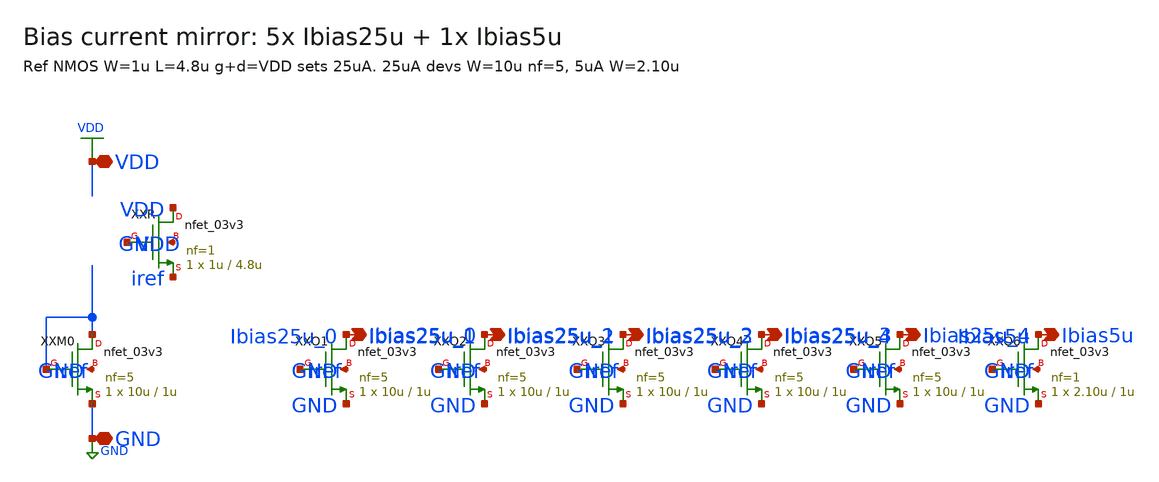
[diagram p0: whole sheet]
** sch_path: ps-bias/bias.sch
**.subckt bias Ibias25u_0 Ibias25u_1 Ibias25u_2 Ibias25u_3 Ibias25u_4 Ibias5u VDD GND
*.opin Ibias25u_0
*.opin Ibias25u_1
*.opin Ibias25u_2
*.opin Ibias25u_3
*.opin Ibias25u_4
*.opin Ibias5u
*.iopin VDD
*.iopin GND
XXR VDD VDD iref GND nfet_03v3 L=4.8u W=1u nf=1 ad='int((nf+1)/2) * W/nf * 0.18u' as='int((nf+2)/2) * W/nf * 0.18u'
+ pd='2*int((nf+1)/2) * (W/nf + 0.18u)' ps='2*int((nf+2)/2) * (W/nf + 0.18u)' nrd='0.18u / W' nrs='0.18u / W'
+ sa=0 sb=0 sd=0 m=1
XXM0 iref iref GND GND nfet_03v3 L=1u W=10u nf=5 ad='int((nf+1)/2) * W/nf * 0.18u' as='int((nf+2)/2) * W/nf * 0.18u'
+ pd='2*int((nf+1)/2) * (W/nf + 0.18u)' ps='2*int((nf+2)/2) * (W/nf + 0.18u)' nrd='0.18u / W' nrs='0.18u / W'
+ sa=0 sb=0 sd=0 m=1
XXO1 Ibias25u_0 iref GND GND nfet_03v3 L=1u W=10u nf=5 ad='int((nf+1)/2) * W/nf * 0.18u' as='int((nf+2)/2) * W/nf * 0.18u'
+ pd='2*int((nf+1)/2) * (W/nf + 0.18u)' ps='2*int((nf+2)/2) * (W/nf + 0.18u)' nrd='0.18u / W' nrs='0.18u / W'
+ sa=0 sb=0 sd=0 m=1
XXO2 Ibias25u_1 iref GND GND nfet_03v3 L=1u W=10u nf=5 ad='int((nf+1)/2) * W/nf * 0.18u' as='int((nf+2)/2) * W/nf * 0.18u'
+ pd='2*int((nf+1)/2) * (W/nf + 0.18u)' ps='2*int((nf+2)/2) * (W/nf + 0.18u)' nrd='0.18u / W' nrs='0.18u / W'
+ sa=0 sb=0 sd=0 m=1
XXO3 Ibias25u_2 iref GND GND nfet_03v3 L=1u W=10u nf=5 ad='int((nf+1)/2) * W/nf * 0.18u' as='int((nf+2)/2) * W/nf * 0.18u'
+ pd='2*int((nf+1)/2) * (W/nf + 0.18u)' ps='2*int((nf+2)/2) * (W/nf + 0.18u)' nrd='0.18u / W' nrs='0.18u / W'
+ sa=0 sb=0 sd=0 m=1
XXO4 Ibias25u_3 iref GND GND nfet_03v3 L=1u W=10u nf=5 ad='int((nf+1)/2) * W/nf * 0.18u' as='int((nf+2)/2) * W/nf * 0.18u'
+ pd='2*int((nf+1)/2) * (W/nf + 0.18u)' ps='2*int((nf+2)/2) * (W/nf + 0.18u)' nrd='0.18u / W' nrs='0.18u / W'
+ sa=0 sb=0 sd=0 m=1
XXO5 Ibias25u_4 iref GND GND nfet_03v3 L=1u W=10u nf=5 ad='int((nf+1)/2) * W/nf * 0.18u' as='int((nf+2)/2) * W/nf * 0.18u'
+ pd='2*int((nf+1)/2) * (W/nf + 0.18u)' ps='2*int((nf+2)/2) * (W/nf + 0.18u)' nrd='0.18u / W' nrs='0.18u / W'
+ sa=0 sb=0 sd=0 m=1
XXO6 Ibias5u iref GND GND nfet_03v3 L=1u W=2.10u nf=1 ad='int((nf+1)/2) * W/nf * 0.18u' as='int((nf+2)/2) * W/nf * 0.18u'
+ pd='2*int((nf+1)/2) * (W/nf + 0.18u)' ps='2*int((nf+2)/2) * (W/nf + 0.18u)' nrd='0.18u / W' nrs='0.18u / W'
+ sa=0 sb=0 sd=0 m=1
**.ends
.GLOBAL VDD
.GLOBAL GND
.end
